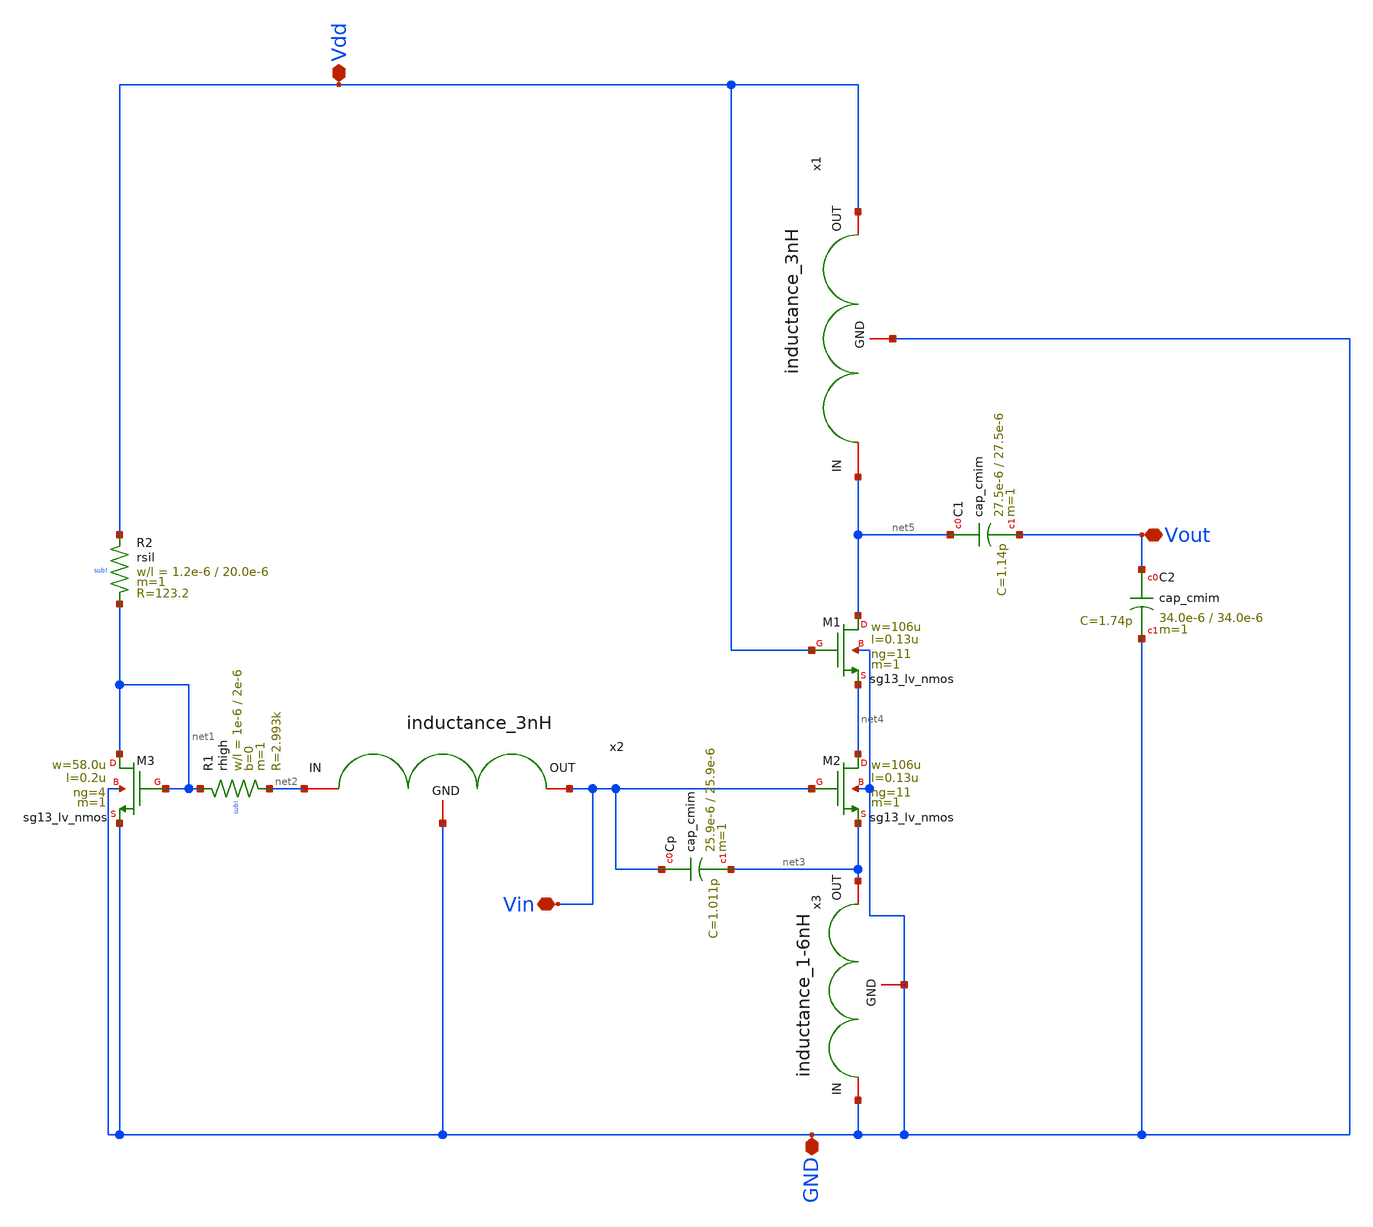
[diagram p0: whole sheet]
** sch_path: LNA_Ind_degen/LNA_xschem.sch
**.subckt LNA_xschem Vout Vin GND Vdd
*.iopin Vout
*.iopin Vin
*.iopin GND
*.iopin Vdd
XC1 net5 Vout cap_cmim w=27.5e-6 l=27.5e-6 m=1 mm_ok=1
XM1 net5 Vdd net4 GND sg13_lv_nmos w=106u l=0.13u ng=11 m=1 mm_ok=1
XR1 net1 net2 sub! rhigh w=1e-6 l=2e-6 m=1 b=0 mm_ok=1
XR2 Vdd net1 sub! rsil w=1.2e-6 l=20.0e-6 m=1 mm_ok=1
x1 Vdd net5 GND inductance_3nH
XM2 net4 Vin net3 GND sg13_lv_nmos w=106u l=0.13u ng=11 m=1 mm_ok=1
XM3 net1 net1 GND GND sg13_lv_nmos w=58.0u l=0.2u ng=4 m=1 mm_ok=1
x2 Vin net2 GND inductance_3nH
x3 net3 GND GND inductance_1-6nH
XC2 Vout GND cap_cmim w=34.0e-6 l=34.0e-6 m=1 mm_ok=1
XCp Vin net3 cap_cmim w=25.9e-6 l=25.9e-6 m=1 mm_ok=1
**.ends

* expanding   symbol:  Zigbee/Inductance/MODEL_XSCHEM/inductance_3nH.sym # of pins=3
** sym_path: Inductance/MODEL_XSCHEM/inductance_3nH.sym
** sch_path: Inductance/MODEL_XSCHEM/inductance_3nH.sch
.subckt inductance_3nH OUT IN GND
*.iopin GND
*.iopin OUT
*.iopin IN
Ls net1 OUT 2.885n m=1
Cox1 IN net2 55.8f m=1
Cox2 OUT net3 55.8f m=1
Csp IN OUT 13.69f m=1
Rp1 net2 GND 18.32 m=1
Rp2 net3 GND 18.32 m=1
Rs IN net1 3.623 m=1
.ends


* expanding   symbol:  Zigbee/Inductance/MODEL_XSCHEM/inductance_1-6nH.sym # of pins=3
** sym_path: Inductance/MODEL_XSCHEM/inductance_1-6nH.sym
** sch_path: Inductance/MODEL_XSCHEM/inductance_1-6nH.sch
.subckt inductance_1-6nH OUT IN GND
*.iopin GND
*.iopin OUT
*.iopin IN
Ls net1 OUT 1.65n m=1
Cox1 IN net2 10f m=1
Cox2 OUT net3 10f m=1
Csp IN OUT 25.785f m=1
Rp1 net2 GND 72.575 m=1
Rp2 net3 GND 72.575 m=1
Rs IN net1 2.27 m=1
.ends

.end
